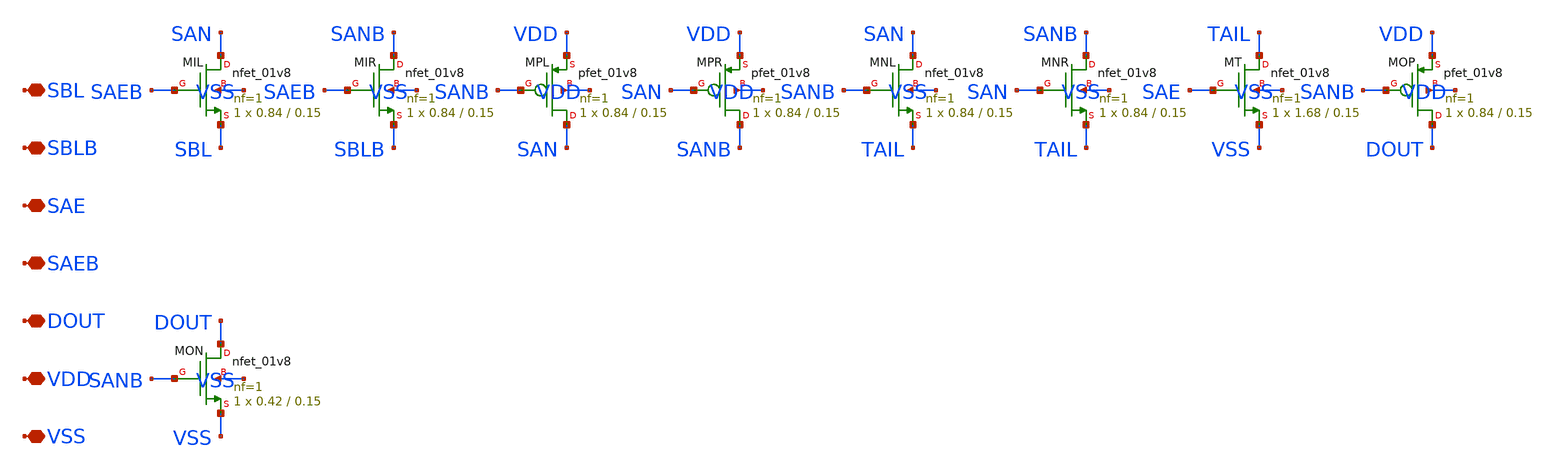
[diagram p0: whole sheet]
** sch_path: design/compiler/cells/sram_senseamp.sch
**.subckt sram_senseamp SBL SBLB SAE SAEB DOUT VDD VSS
*.iopin SBL
*.iopin SBLB
*.iopin SAE
*.iopin SAEB
*.iopin DOUT
*.iopin VDD
*.iopin VSS
XMIL SAN SAEB SBL VSS sky130_fd_pr__nfet_01v8 L=0.15 W=0.84 nf=1 ad=0.2436 as=0.2436 pd=2.26 ps=2.26
+ nrd=0.3452 nrs=0.3452 sa=0 sb=0 sd=0 mult=1 m=1
XMIR SANB SAEB SBLB VSS sky130_fd_pr__nfet_01v8 L=0.15 W=0.84 nf=1 ad=0.2436 as=0.2436 pd=2.26
+ ps=2.26 nrd=0.3452 nrs=0.3452 sa=0 sb=0 sd=0 mult=1 m=1
XMPL SAN SANB VDD VDD sky130_fd_pr__pfet_01v8 L=0.15 W=0.84 nf=1 ad=0.2436 as=0.2436 pd=2.26 ps=2.26
+ nrd=0.3452 nrs=0.3452 sa=0 sb=0 sd=0 mult=1 m=1
XMPR SANB SAN VDD VDD sky130_fd_pr__pfet_01v8 L=0.15 W=0.84 nf=1 ad=0.2436 as=0.2436 pd=2.26 ps=2.26
+ nrd=0.3452 nrs=0.3452 sa=0 sb=0 sd=0 mult=1 m=1
XMNL SAN SANB TAIL VSS sky130_fd_pr__nfet_01v8 L=0.15 W=0.84 nf=1 ad=0.2436 as=0.2436 pd=2.26
+ ps=2.26 nrd=0.3452 nrs=0.3452 sa=0 sb=0 sd=0 mult=1 m=1
XMNR SANB SAN TAIL VSS sky130_fd_pr__nfet_01v8 L=0.15 W=0.84 nf=1 ad=0.2436 as=0.2436 pd=2.26
+ ps=2.26 nrd=0.3452 nrs=0.3452 sa=0 sb=0 sd=0 mult=1 m=1
XMT TAIL SAE VSS VSS sky130_fd_pr__nfet_01v8 L=0.15 W=1.68 nf=1 ad=0.4872 as=0.4872 pd=3.94 ps=3.94
+ nrd=0.1726 nrs=0.1726 sa=0 sb=0 sd=0 mult=1 m=1
XMOP DOUT SANB VDD VDD sky130_fd_pr__pfet_01v8 L=0.15 W=0.84 nf=1 ad=0.2436 as=0.2436 pd=2.26
+ ps=2.26 nrd=0.3452 nrs=0.3452 sa=0 sb=0 sd=0 mult=1 m=1
XMON DOUT SANB VSS VSS sky130_fd_pr__nfet_01v8 L=0.15 W=0.42 nf=1 ad=0.1218 as=0.1218 pd=1.42
+ ps=1.42 nrd=0.6905 nrs=0.6905 sa=0 sb=0 sd=0 mult=1 m=1
**.ends
.end
